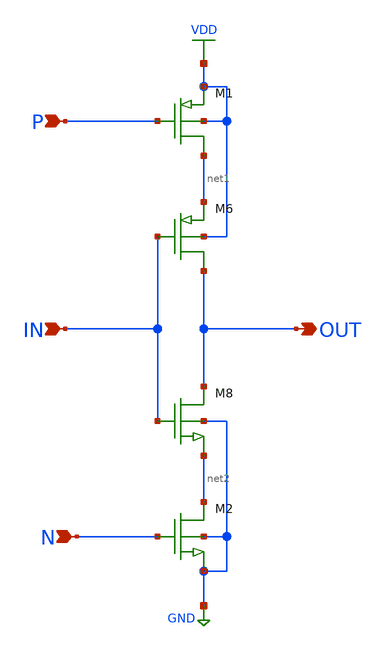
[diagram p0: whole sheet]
** sch_path: task_LATCH/CLOCKEDINVERTER.sch
**.subckt CLOCKEDINVERTER OUT IN P N
*.opin OUT
*.ipin IN
*.ipin P
*.ipin N
M6 OUT IN net1 VDD pch w=10.5u l=0.35u as=0 ps=0 ad=0 pd=0 m=1
M8 OUT IN net2 GND nch w=3.5u l=0.35u as=0 ps=0 ad=0 pd=0 m=1
M1 net1 P VDD VDD pch w=10.5u l=0.35u as=0 ps=0 ad=0 pd=0 m=1
M2 net2 N GND GND nch w=3.5u l=0.35u as=0 ps=0 ad=0 pd=0 m=1
**.ends
.GLOBAL VDD
.GLOBAL GND
.end
